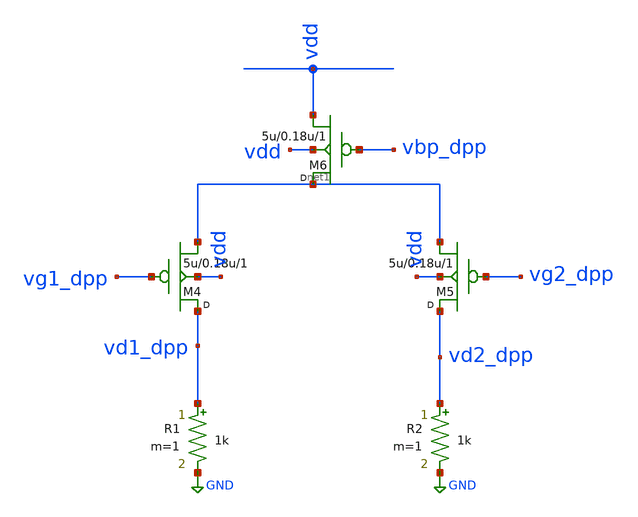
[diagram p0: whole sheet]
** sch_path: synthetic/blocks/diff_pair_pmos.sch
**.subckt diff_pair_pmos
M4 vd1_dpp vg1_dpp net1 vdd pmos w=5u l=0.18u m=1
M5 vd2_dpp vg2_dpp net1 vdd pmos w=5u l=0.18u m=1
M6 net1 vbp_dpp vdd vdd pmos w=5u l=0.18u m=1
R1 vd1_dpp GND 1k m=1
R2 vd2_dpp GND 1k m=1
**.ends
.GLOBAL GND
.end
